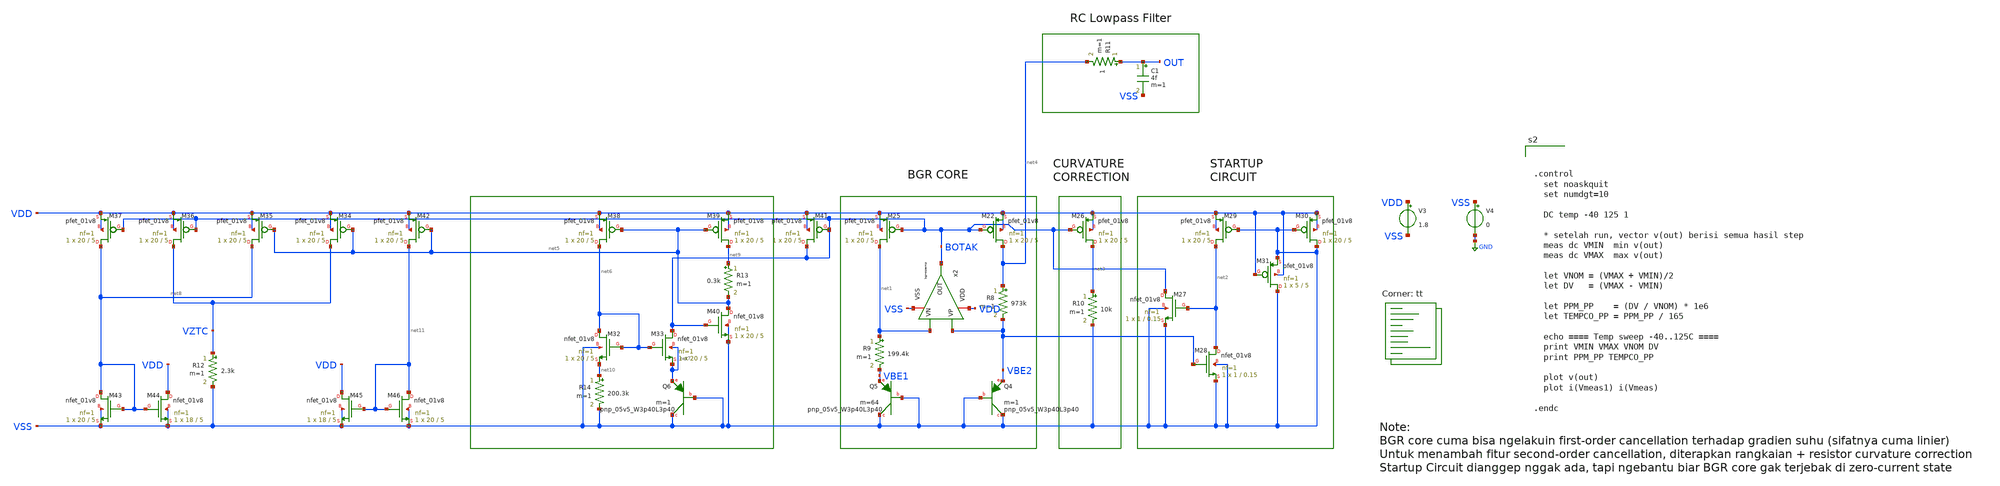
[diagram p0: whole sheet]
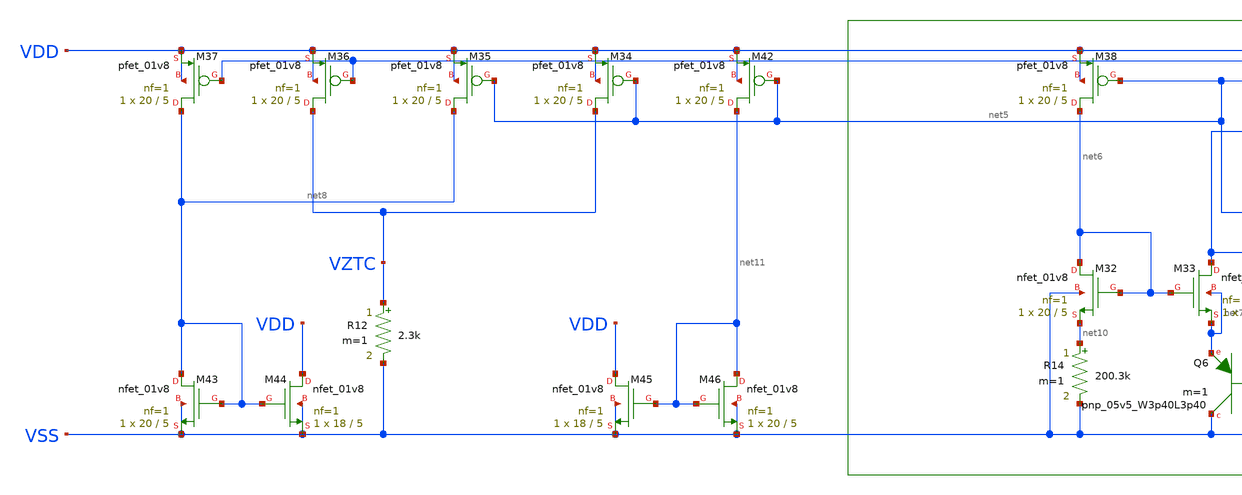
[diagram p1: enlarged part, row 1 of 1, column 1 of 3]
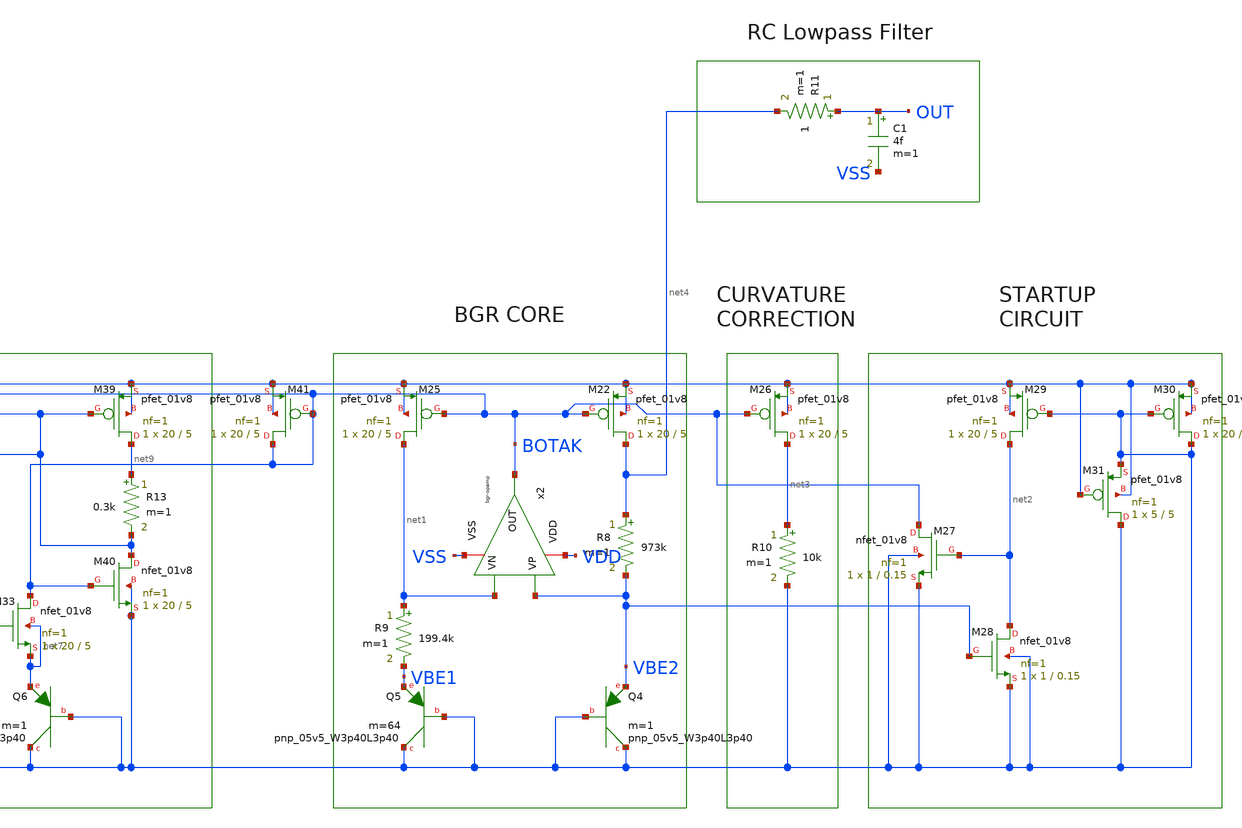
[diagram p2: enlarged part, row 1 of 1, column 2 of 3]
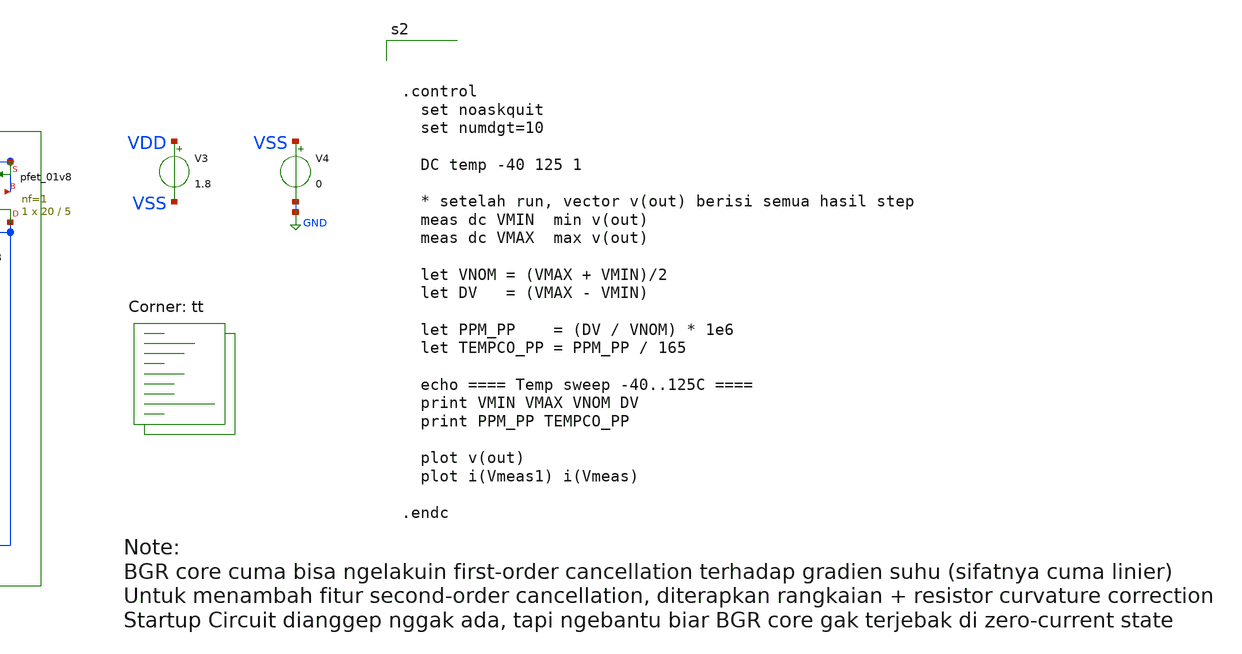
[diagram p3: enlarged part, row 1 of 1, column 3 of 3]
** sch_path: bandgap/bgr-final/tb_bgr-vref.sch
**.subckt tb_bgr-vref
V3 VDD VSS 1.8
V4 VSS GND 0
x2 VDD BOTAK VBE2 net1 VSS bgr-opamp
XM22 net4 BOTAK VDD VDD sky130_fd_pr__pfet_01v8 L=5 W=20 nf=1 ad='int((nf+1)/2) * W/nf * 0.29' as='int((nf+2)/2) * W/nf * 0.29'
+ pd='2*int((nf+1)/2) * (W/nf + 0.29)' ps='2*int((nf+2)/2) * (W/nf + 0.29)' nrd='0.29 / W' nrs='0.29 / W'
+ sa=0 sb=0 sd=0 mult=1 m=1
XM25 net1 BOTAK VDD VDD sky130_fd_pr__pfet_01v8 L=5 W=20 nf=1 ad='int((nf+1)/2) * W/nf * 0.29' as='int((nf+2)/2) * W/nf * 0.29'
+ pd='2*int((nf+1)/2) * (W/nf + 0.29)' ps='2*int((nf+2)/2) * (W/nf + 0.29)' nrd='0.29 / W' nrs='0.29 / W'
+ sa=0 sb=0 sd=0 mult=1 m=1
R8 net4 VBE2 973k m=1
R9 net1 VBE1 199.4k m=1
XQ4 VSS VSS VBE2 sky130_fd_pr__pnp_05v5_W3p40L3p40 m=1
XQ5 VSS VSS VBE1 sky130_fd_pr__pnp_05v5_W3p40L3p40 m=64
XM26 net3 BOTAK VDD VDD sky130_fd_pr__pfet_01v8 L=5 W=20 nf=1 ad='int((nf+1)/2) * W/nf * 0.29' as='int((nf+2)/2) * W/nf * 0.29'
+ pd='2*int((nf+1)/2) * (W/nf + 0.29)' ps='2*int((nf+2)/2) * (W/nf + 0.29)' nrd='0.29 / W' nrs='0.29 / W'
+ sa=0 sb=0 sd=0 mult=1 m=1
R10 net3 VSS 10k m=1
XM27 BOTAK net2 VSS VSS sky130_fd_pr__nfet_01v8 L=0.15 W=1 nf=1 ad='int((nf+1)/2) * W/nf * 0.29' as='int((nf+2)/2) * W/nf * 0.29'
+ pd='2*int((nf+1)/2) * (W/nf + 0.29)' ps='2*int((nf+2)/2) * (W/nf + 0.29)' nrd='0.29 / W' nrs='0.29 / W'
+ sa=0 sb=0 sd=0 mult=1 m=1
XM28 net2 VBE2 VSS VSS sky130_fd_pr__nfet_01v8 L=0.15 W=1 nf=1 ad='int((nf+1)/2) * W/nf * 0.29' as='int((nf+2)/2) * W/nf * 0.29'
+ pd='2*int((nf+1)/2) * (W/nf + 0.29)' ps='2*int((nf+2)/2) * (W/nf + 0.29)' nrd='0.29 / W' nrs='0.29 / W'
+ sa=0 sb=0 sd=0 mult=1 m=1
XM29 net2 VSS VDD VDD sky130_fd_pr__pfet_01v8 L=5 W=20 nf=1 ad='int((nf+1)/2) * W/nf * 0.29' as='int((nf+2)/2) * W/nf * 0.29'
+ pd='2*int((nf+1)/2) * (W/nf + 0.29)' ps='2*int((nf+2)/2) * (W/nf + 0.29)' nrd='0.29 / W' nrs='0.29 / W'
+ sa=0 sb=0 sd=0 mult=1 m=1
XM30 VSS VSS VDD VDD sky130_fd_pr__pfet_01v8 L=5 W=20 nf=1 ad='int((nf+1)/2) * W/nf * 0.29' as='int((nf+2)/2) * W/nf * 0.29'
+ pd='2*int((nf+1)/2) * (W/nf + 0.29)' ps='2*int((nf+2)/2) * (W/nf + 0.29)' nrd='0.29 / W' nrs='0.29 / W'
+ sa=0 sb=0 sd=0 mult=1 m=1
XM31 VSS VDD VSS VDD sky130_fd_pr__pfet_01v8 L=5 W=5 nf=1 ad='int((nf+1)/2) * W/nf * 0.29' as='int((nf+2)/2) * W/nf * 0.29'
+ pd='2*int((nf+1)/2) * (W/nf + 0.29)' ps='2*int((nf+2)/2) * (W/nf + 0.29)' nrd='0.29 / W' nrs='0.29 / W'
+ sa=0 sb=0 sd=0 mult=1 m=1
C1 OUT VSS 4f m=1
R11 OUT net4 1 m=1
XM32 net6 net6 net10 VSS sky130_fd_pr__nfet_01v8 L=5 W=20 nf=1 ad='int((nf+1)/2) * W/nf * 0.29' as='int((nf+2)/2) * W/nf * 0.29'
+ pd='2*int((nf+1)/2) * (W/nf + 0.29)' ps='2*int((nf+2)/2) * (W/nf + 0.29)' nrd='0.29 / W' nrs='0.29 / W'
+ sa=0 sb=0 sd=0 mult=1 m=1
XM33 BOTAK net6 net7 net7 sky130_fd_pr__nfet_01v8 L=5 W=20 nf=1 ad='int((nf+1)/2) * W/nf * 0.29' as='int((nf+2)/2) * W/nf * 0.29'
+ pd='2*int((nf+1)/2) * (W/nf + 0.29)' ps='2*int((nf+2)/2) * (W/nf + 0.29)' nrd='0.29 / W' nrs='0.29 / W'
+ sa=0 sb=0 sd=0 mult=1 m=1
XQ6 VSS VSS net7 sky130_fd_pr__pnp_05v5_W3p40L3p40 m=1
XM34 VZTC net5 VDD VDD sky130_fd_pr__pfet_01v8 L=5 W=20 nf=1 ad='int((nf+1)/2) * W/nf * 0.29' as='int((nf+2)/2) * W/nf * 0.29'
+ pd='2*int((nf+1)/2) * (W/nf + 0.29)' ps='2*int((nf+2)/2) * (W/nf + 0.29)' nrd='0.29 / W' nrs='0.29 / W'
+ sa=0 sb=0 sd=0 mult=1 m=1
XM35 net8 net5 VDD VDD sky130_fd_pr__pfet_01v8 L=5 W=20 nf=1 ad='int((nf+1)/2) * W/nf * 0.29' as='int((nf+2)/2) * W/nf * 0.29'
+ pd='2*int((nf+1)/2) * (W/nf + 0.29)' ps='2*int((nf+2)/2) * (W/nf + 0.29)' nrd='0.29 / W' nrs='0.29 / W'
+ sa=0 sb=0 sd=0 mult=1 m=1
XM36 VZTC BOTAK VDD VDD sky130_fd_pr__pfet_01v8 L=5 W=20 nf=1 ad='int((nf+1)/2) * W/nf * 0.29' as='int((nf+2)/2) * W/nf * 0.29'
+ pd='2*int((nf+1)/2) * (W/nf + 0.29)' ps='2*int((nf+2)/2) * (W/nf + 0.29)' nrd='0.29 / W' nrs='0.29 / W'
+ sa=0 sb=0 sd=0 mult=1 m=1
XM37 net8 BOTAK VDD VDD sky130_fd_pr__pfet_01v8 L=5 W=20 nf=1 ad='int((nf+1)/2) * W/nf * 0.29' as='int((nf+2)/2) * W/nf * 0.29'
+ pd='2*int((nf+1)/2) * (W/nf + 0.29)' ps='2*int((nf+2)/2) * (W/nf + 0.29)' nrd='0.29 / W' nrs='0.29 / W'
+ sa=0 sb=0 sd=0 mult=1 m=1
R12 VZTC VSS 2.3k m=1
XM38 net6 net5 VDD VDD sky130_fd_pr__pfet_01v8 L=5 W=20 nf=1 ad='int((nf+1)/2) * W/nf * 0.29' as='int((nf+2)/2) * W/nf * 0.29'
+ pd='2*int((nf+1)/2) * (W/nf + 0.29)' ps='2*int((nf+2)/2) * (W/nf + 0.29)' nrd='0.29 / W' nrs='0.29 / W'
+ sa=0 sb=0 sd=0 mult=1 m=1
XM39 net9 net5 VDD VDD sky130_fd_pr__pfet_01v8 L=5 W=20 nf=1 ad='int((nf+1)/2) * W/nf * 0.29' as='int((nf+2)/2) * W/nf * 0.29'
+ pd='2*int((nf+1)/2) * (W/nf + 0.29)' ps='2*int((nf+2)/2) * (W/nf + 0.29)' nrd='0.29 / W' nrs='0.29 / W'
+ sa=0 sb=0 sd=0 mult=1 m=1
R13 net9 net5 0.3k m=1
XM40 net5 BOTAK VSS VSS sky130_fd_pr__nfet_01v8 L=5 W=20 nf=1 ad='int((nf+1)/2) * W/nf * 0.29' as='int((nf+2)/2) * W/nf * 0.29'
+ pd='2*int((nf+1)/2) * (W/nf + 0.29)' ps='2*int((nf+2)/2) * (W/nf + 0.29)' nrd='0.29 / W' nrs='0.29 / W'
+ sa=0 sb=0 sd=0 mult=1 m=1
XM41 BOTAK BOTAK VDD VDD sky130_fd_pr__pfet_01v8 L=5 W=20 nf=1 ad='int((nf+1)/2) * W/nf * 0.29' as='int((nf+2)/2) * W/nf * 0.29'
+ pd='2*int((nf+1)/2) * (W/nf + 0.29)' ps='2*int((nf+2)/2) * (W/nf + 0.29)' nrd='0.29 / W' nrs='0.29 / W'
+ sa=0 sb=0 sd=0 mult=1 m=1
R14 net10 VSS 200.3k m=1
XM42 net11 net5 VDD VDD sky130_fd_pr__pfet_01v8 L=5 W=20 nf=1 ad='int((nf+1)/2) * W/nf * 0.29' as='int((nf+2)/2) * W/nf * 0.29'
+ pd='2*int((nf+1)/2) * (W/nf + 0.29)' ps='2*int((nf+2)/2) * (W/nf + 0.29)' nrd='0.29 / W' nrs='0.29 / W'
+ sa=0 sb=0 sd=0 mult=1 m=1
XM43 net8 net8 VSS VSS sky130_fd_pr__nfet_01v8 L=5 W=20 nf=1 ad='int((nf+1)/2) * W/nf * 0.29' as='int((nf+2)/2) * W/nf * 0.29'
+ pd='2*int((nf+1)/2) * (W/nf + 0.29)' ps='2*int((nf+2)/2) * (W/nf + 0.29)' nrd='0.29 / W' nrs='0.29 / W'
+ sa=0 sb=0 sd=0 mult=1 m=1
XM44 VDD net8 VSS VSS sky130_fd_pr__nfet_01v8 L=5 W=18 nf=1 ad='int((nf+1)/2) * W/nf * 0.29' as='int((nf+2)/2) * W/nf * 0.29'
+ pd='2*int((nf+1)/2) * (W/nf + 0.29)' ps='2*int((nf+2)/2) * (W/nf + 0.29)' nrd='0.29 / W' nrs='0.29 / W'
+ sa=0 sb=0 sd=0 mult=1 m=1
XM45 VDD net11 VSS VSS sky130_fd_pr__nfet_01v8 L=5 W=18 nf=1 ad='int((nf+1)/2) * W/nf * 0.29' as='int((nf+2)/2) * W/nf * 0.29'
+ pd='2*int((nf+1)/2) * (W/nf + 0.29)' ps='2*int((nf+2)/2) * (W/nf + 0.29)' nrd='0.29 / W' nrs='0.29 / W'
+ sa=0 sb=0 sd=0 mult=1 m=1
XM46 net11 net11 VSS VSS sky130_fd_pr__nfet_01v8 L=5 W=20 nf=1 ad='int((nf+1)/2) * W/nf * 0.29' as='int((nf+2)/2) * W/nf * 0.29'
+ pd='2*int((nf+1)/2) * (W/nf + 0.29)' ps='2*int((nf+2)/2) * (W/nf + 0.29)' nrd='0.29 / W' nrs='0.29 / W'
+ sa=0 sb=0 sd=0 mult=1 m=1
**** begin user architecture code
.lib $::SKYWATER_MODELS/sky130.lib.spice tt



.control
  set noaskquit
  set numdgt=10

  DC temp -40 125 1

  * setelah run, vector v(out) berisi semua hasil step
  meas dc VMIN  min v(out)
  meas dc VMAX  max v(out)

  let VNOM = (VMAX + VMIN)/2
  let DV   = (VMAX - VMIN)

  let PPM_PP    = (DV / VNOM) * 1e6
  let TEMPCO_PP = PPM_PP / 165

  echo ==== Temp sweep -40..125C ====
  print VMIN VMAX VNOM DV
  print PPM_PP TEMPCO_PP

  plot v(out)
  plot i(Vmeas1) i(Vmeas)

.endc


**** end user architecture code
**.ends

* expanding   symbol:  afe-icdec-teknofest-2026/bandgap/bgr-opamp/bgr-opamp.sym # of pins=5
** sym_path: bandgap/bgr-opamp/bgr-opamp.sym
** sch_path: bandgap/bgr-opamp/bgr-opamp.sch
.subckt bgr-opamp VDD OUT VP VN VSS
*.iopin VSS
*.iopin VDD
*.ipin VP
*.ipin VN
*.opin OUT
XM1 net1 VP net3 VSS sky130_fd_pr__nfet_01v8 L=0.3 W=2.5 nf=2 ad='int((nf+1)/2) * W/nf * 0.29' as='int((nf+2)/2) * W/nf * 0.29'
+ pd='2*int((nf+1)/2) * (W/nf + 0.29)' ps='2*int((nf+2)/2) * (W/nf + 0.29)' nrd='0.29 / W' nrs='0.29 / W'
+ sa=0 sb=0 sd=0 mult=1 m=1
XM2 net2 VN net3 VSS sky130_fd_pr__nfet_01v8 L=0.3 W=2.5 nf=2 ad='int((nf+1)/2) * W/nf * 0.29' as='int((nf+2)/2) * W/nf * 0.29'
+ pd='2*int((nf+1)/2) * (W/nf + 0.29)' ps='2*int((nf+2)/2) * (W/nf + 0.29)' nrd='0.29 / W' nrs='0.29 / W'
+ sa=0 sb=0 sd=0 mult=1 m=1
XM4 net2 net1 VDD VDD sky130_fd_pr__pfet_01v8 L=1.25 W=10.8 nf=4 ad='int((nf+1)/2) * W/nf * 0.29' as='int((nf+2)/2) * W/nf * 0.29'
+ pd='2*int((nf+1)/2) * (W/nf + 0.29)' ps='2*int((nf+2)/2) * (W/nf + 0.29)' nrd='0.29 / W' nrs='0.29 / W'
+ sa=0 sb=0 sd=0 mult=1 m=1
XM3 net1 net1 VDD VDD sky130_fd_pr__pfet_01v8 L=1.25 W=10.8 nf=4 ad='int((nf+1)/2) * W/nf * 0.29' as='int((nf+2)/2) * W/nf * 0.29'
+ pd='2*int((nf+1)/2) * (W/nf + 0.29)' ps='2*int((nf+2)/2) * (W/nf + 0.29)' nrd='0.29 / W' nrs='0.29 / W'
+ sa=0 sb=0 sd=0 mult=1 m=1
XM5 net3 net4 VSS VSS sky130_fd_pr__nfet_01v8 L=1.25 W=3.4 nf=1 ad='int((nf+1)/2) * W/nf * 0.29' as='int((nf+2)/2) * W/nf * 0.29'
+ pd='2*int((nf+1)/2) * (W/nf + 0.29)' ps='2*int((nf+2)/2) * (W/nf + 0.29)' nrd='0.29 / W' nrs='0.29 / W'
+ sa=0 sb=0 sd=0 mult=1 m=1
XM9 net4 net5 net10 VSS sky130_fd_pr__nfet_01v8 L=1.25 W=3.4 nf=1 ad='int((nf+1)/2) * W/nf * 0.29' as='int((nf+2)/2) * W/nf * 0.29'
+ pd='2*int((nf+1)/2) * (W/nf + 0.29)' ps='2*int((nf+2)/2) * (W/nf + 0.29)' nrd='0.29 / W' nrs='0.29 / W'
+ sa=0 sb=0 sd=0 mult=1 m=1
XM8 net4 net4 VDD VDD sky130_fd_pr__pfet_01v8 L=1.25 W=10.8 nf=4 ad='int((nf+1)/2) * W/nf * 0.29' as='int((nf+2)/2) * W/nf * 0.29'
+ pd='2*int((nf+1)/2) * (W/nf + 0.29)' ps='2*int((nf+2)/2) * (W/nf + 0.29)' nrd='0.29 / W' nrs='0.29 / W'
+ sa=0 sb=0 sd=0 mult=1 m=1
XM11 net5 net4 VDD VDD sky130_fd_pr__pfet_01v8 L=1.25 W=10.8 nf=4 ad='int((nf+1)/2) * W/nf * 0.29' as='int((nf+2)/2) * W/nf * 0.29'
+ pd='2*int((nf+1)/2) * (W/nf + 0.29)' ps='2*int((nf+2)/2) * (W/nf + 0.29)' nrd='0.29 / W' nrs='0.29 / W'
+ sa=0 sb=0 sd=0 mult=1 m=1
XM10 net5 net5 VSS VSS sky130_fd_pr__nfet_01v8 L=1.25 W=3.4 nf=1 ad='int((nf+1)/2) * W/nf * 0.29' as='int((nf+2)/2) * W/nf * 0.29'
+ pd='2*int((nf+1)/2) * (W/nf + 0.29)' ps='2*int((nf+2)/2) * (W/nf + 0.29)' nrd='0.29 / W' nrs='0.29 / W'
+ sa=0 sb=0 sd=0 mult=1 m=1
XM6 OUT net2 VDD VDD sky130_fd_pr__pfet_01v8 L=1.25 W=110 nf=32 ad='int((nf+1)/2) * W/nf * 0.29' as='int((nf+2)/2) * W/nf * 0.29'
+ pd='2*int((nf+1)/2) * (W/nf + 0.29)' ps='2*int((nf+2)/2) * (W/nf + 0.29)' nrd='0.29 / W' nrs='0.29 / W'
+ sa=0 sb=0 sd=0 mult=1 m=1
XM7 OUT net4 VSS VSS sky130_fd_pr__nfet_01v8 L=1.25 W=12 nf=4 ad='int((nf+1)/2) * W/nf * 0.29' as='int((nf+2)/2) * W/nf * 0.29'
+ pd='2*int((nf+1)/2) * (W/nf + 0.29)' ps='2*int((nf+2)/2) * (W/nf + 0.29)' nrd='0.29 / W' nrs='0.29 / W'
+ sa=0 sb=0 sd=0 mult=1 m=1
XC2 OUT net2 sky130_fd_pr__cap_mim_m3_1 W=15 L=15 MF=4 m=4
XM12 net4 net4 net5 VSS sky130_fd_pr__nfet_01v8 L=0.15 W=0.85 nf=1 ad='int((nf+1)/2) * W/nf * 0.29' as='int((nf+2)/2) * W/nf * 0.29'
+ pd='2*int((nf+1)/2) * (W/nf + 0.29)' ps='2*int((nf+2)/2) * (W/nf + 0.29)' nrd='0.29 / W' nrs='0.29 / W'
+ sa=0 sb=0 sd=0 mult=1 m=1
XR2 net6 net10 VSS sky130_fd_pr__res_high_po_1p41 L=3.235 mult=1 m=1
XR3 net8 net6 VSS sky130_fd_pr__res_high_po_1p41 L=3.235 mult=1 m=1
XR4 net7 net8 VSS sky130_fd_pr__res_high_po_1p41 L=3.235 mult=1 m=1
XR5 net9 net7 VSS sky130_fd_pr__res_high_po_1p41 L=3.235 mult=1 m=1
XR6 VSS net9 VSS sky130_fd_pr__res_high_po_1p41 L=3.235 mult=1 m=1
.ends

.GLOBAL GND
.end
